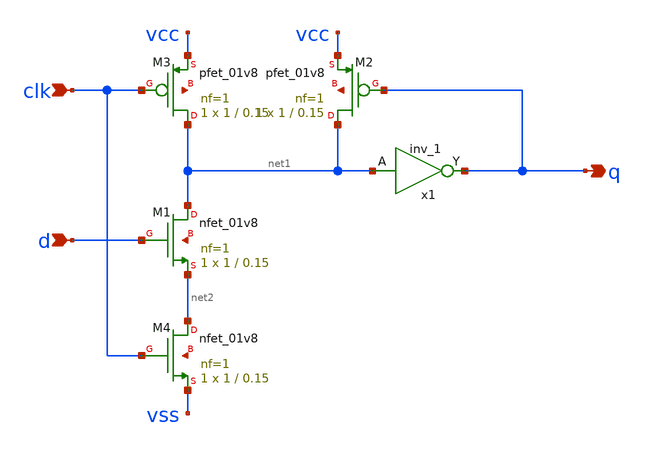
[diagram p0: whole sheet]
** sch_path: src/xe/test_cases/dyn.sch
**.subckt dyn clk q d
*.ipin clk
*.opin q
*.ipin d
x1 net1 vcc vcc vss vss q sky130_fd_sc_hd__inv_1
XM1 net1 d net2 net3 sky130_fd_pr__nfet_01v8 L=0.15 W=1 nf=1 ad='int((nf+1)/2) * W/nf * 0.29' as='int((nf+2)/2) * W/nf * 0.29'
+ pd='2*int((nf+1)/2) * (W/nf + 0.29)' ps='2*int((nf+2)/2) * (W/nf + 0.29)' nrd='0.29 / W' nrs='0.29 / W'
+ sa=0 sb=0 sd=0 mult=1 m=1
XM2 net1 q vcc net4 sky130_fd_pr__pfet_01v8 L=0.15 W=1 nf=1 ad='int((nf+1)/2) * W/nf * 0.29' as='int((nf+2)/2) * W/nf * 0.29'
+ pd='2*int((nf+1)/2) * (W/nf + 0.29)' ps='2*int((nf+2)/2) * (W/nf + 0.29)' nrd='0.29 / W' nrs='0.29 / W'
+ sa=0 sb=0 sd=0 mult=1 m=1
XM3 net1 clk vcc net5 sky130_fd_pr__pfet_01v8 L=0.15 W=1 nf=1 ad='int((nf+1)/2) * W/nf * 0.29' as='int((nf+2)/2) * W/nf * 0.29'
+ pd='2*int((nf+1)/2) * (W/nf + 0.29)' ps='2*int((nf+2)/2) * (W/nf + 0.29)' nrd='0.29 / W' nrs='0.29 / W'
+ sa=0 sb=0 sd=0 mult=1 m=1
XM4 net2 clk vss net6 sky130_fd_pr__nfet_01v8 L=0.15 W=1 nf=1 ad='int((nf+1)/2) * W/nf * 0.29' as='int((nf+2)/2) * W/nf * 0.29'
+ pd='2*int((nf+1)/2) * (W/nf + 0.29)' ps='2*int((nf+2)/2) * (W/nf + 0.29)' nrd='0.29 / W' nrs='0.29 / W'
+ sa=0 sb=0 sd=0 mult=1 m=1
**.ends
.end
